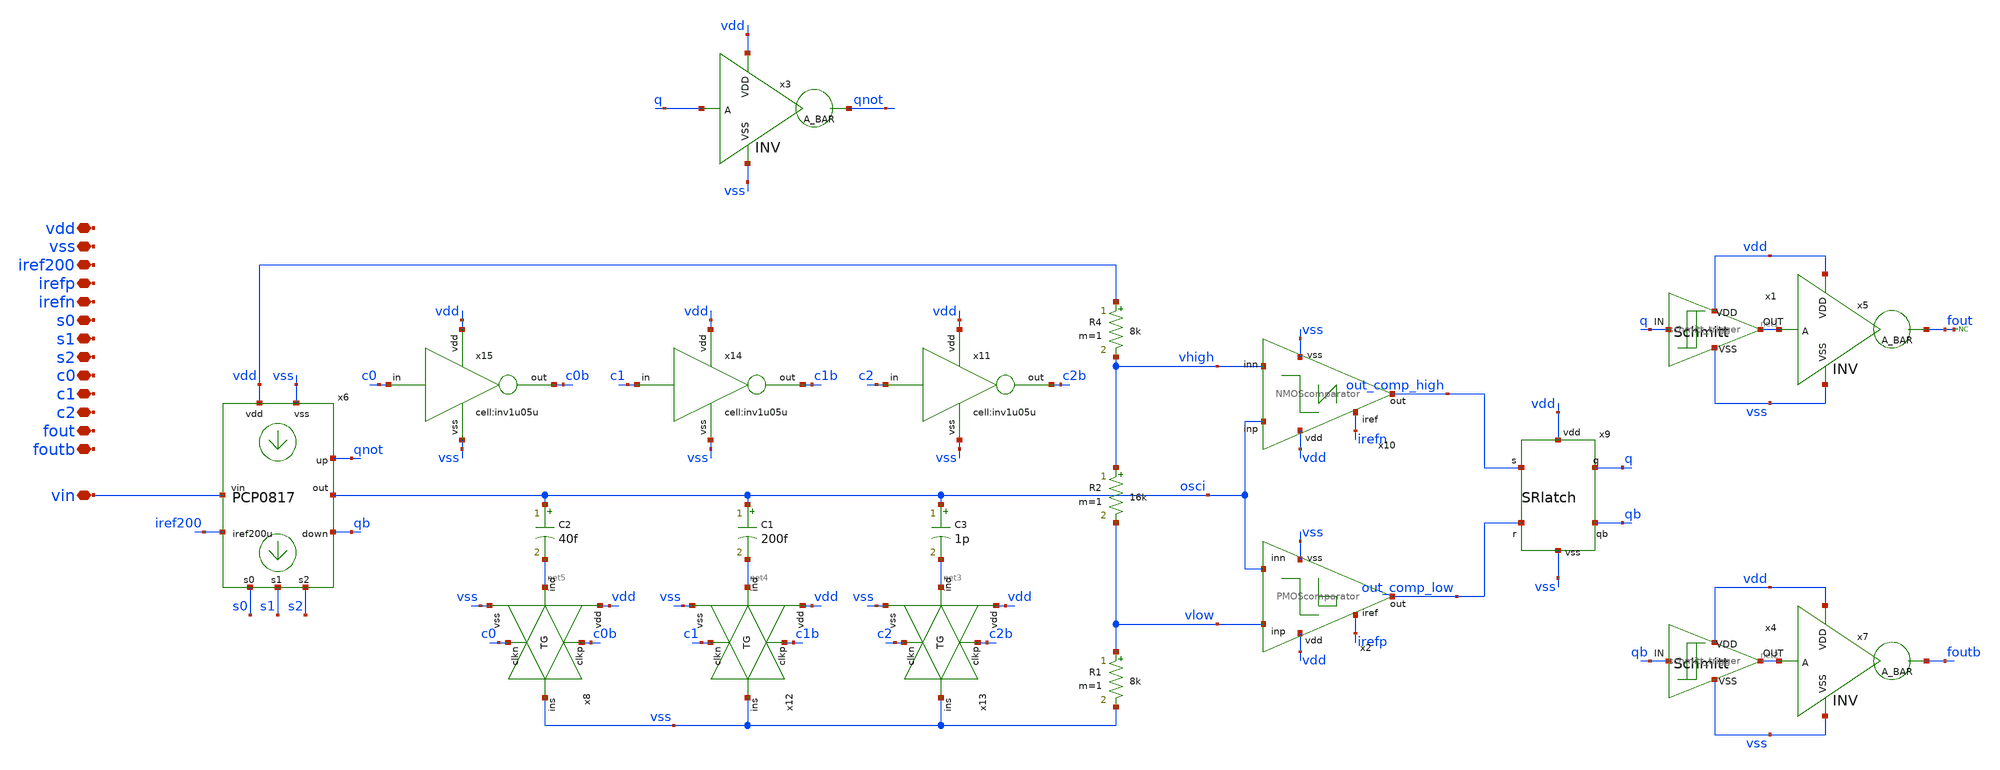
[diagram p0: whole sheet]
** sch_path: designs/libs/qw_core_analog/VCO0831_withTG/VCO0831_withTG.sch
**.subckt VCO0831_withTG vin vdd vss iref200 irefp irefn s0 s1 s2 fout foutb c0 c1 c2
*.iopin vin
*.iopin vdd
*.iopin vss
*.iopin iref200
*.iopin irefp
*.iopin irefn
*.iopin s0
*.iopin s1
*.iopin s2
*.iopin fout
*.iopin foutb
*.iopin c0
*.iopin c1
*.iopin c2
R1 vlow vss 8k m=1
R2 vhigh vlow 16k m=1
R4 vdd vhigh 8k m=1
x9 vdd out_comp_high q qb out_comp_low vss SRlatch
x2 vdd irefp vlow out_comp_low osci vss PMOScomparator
x10 vdd osci out_comp_high vhigh irefn vss NMOScomparator
x3 vdd q qnot vss INV
x1 q net1 vdd vss schmitt_trigger
x4 qb net2 vdd vss schmitt_trigger
x5 vdd net1 fout vss INV
x7 vdd net2 foutb vss INV
* noconn fout
C3 osci net3 1p m=1
x11 c2 vdd c2b vss inv1u05u
x6 vdd vss vin iref200 osci qnot qb s0 s1 s2 PCP0817
C1 osci net4 200f m=1
C2 osci net5 40f m=1
x14 c1 vdd c1b vss inv1u05u
x15 c0 vdd c0b vss inv1u05u
x8 vdd c0b net5 vss vss c0 TG
x12 vdd c1b net4 vss vss c1 TG
x13 vdd c2b net3 vss vss c2 TG
**.ends
.end
